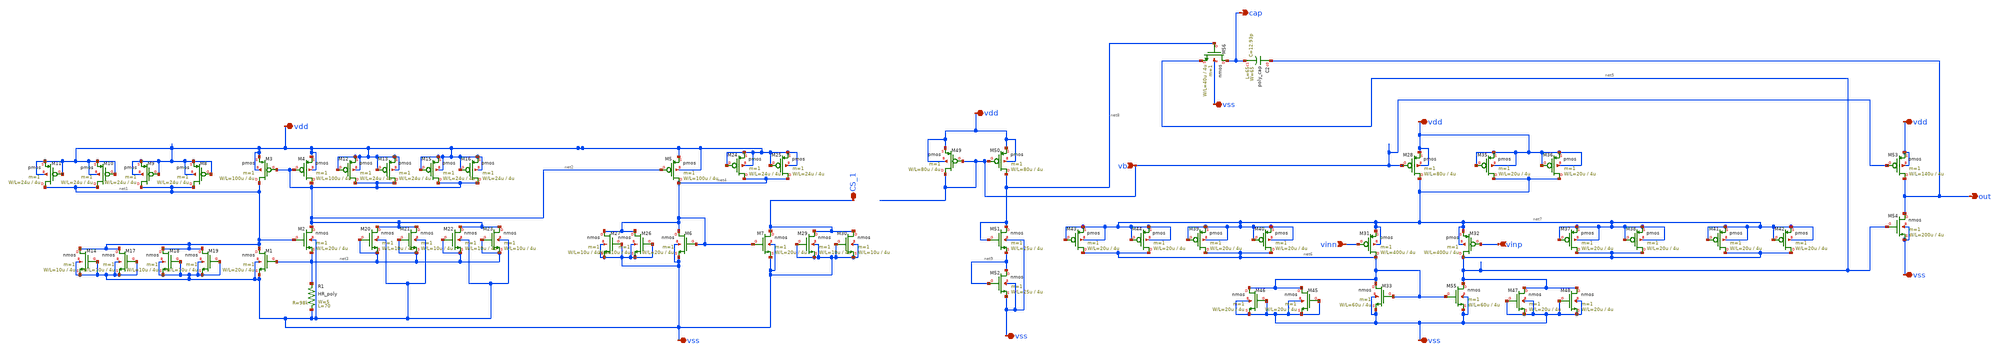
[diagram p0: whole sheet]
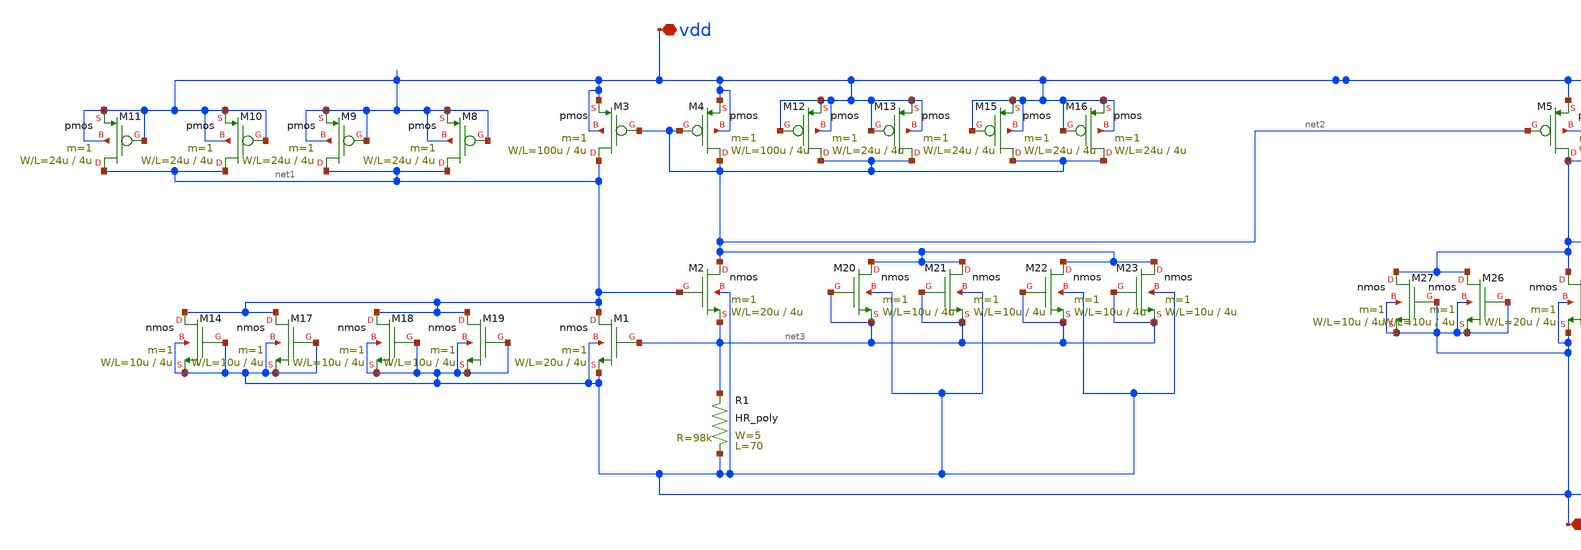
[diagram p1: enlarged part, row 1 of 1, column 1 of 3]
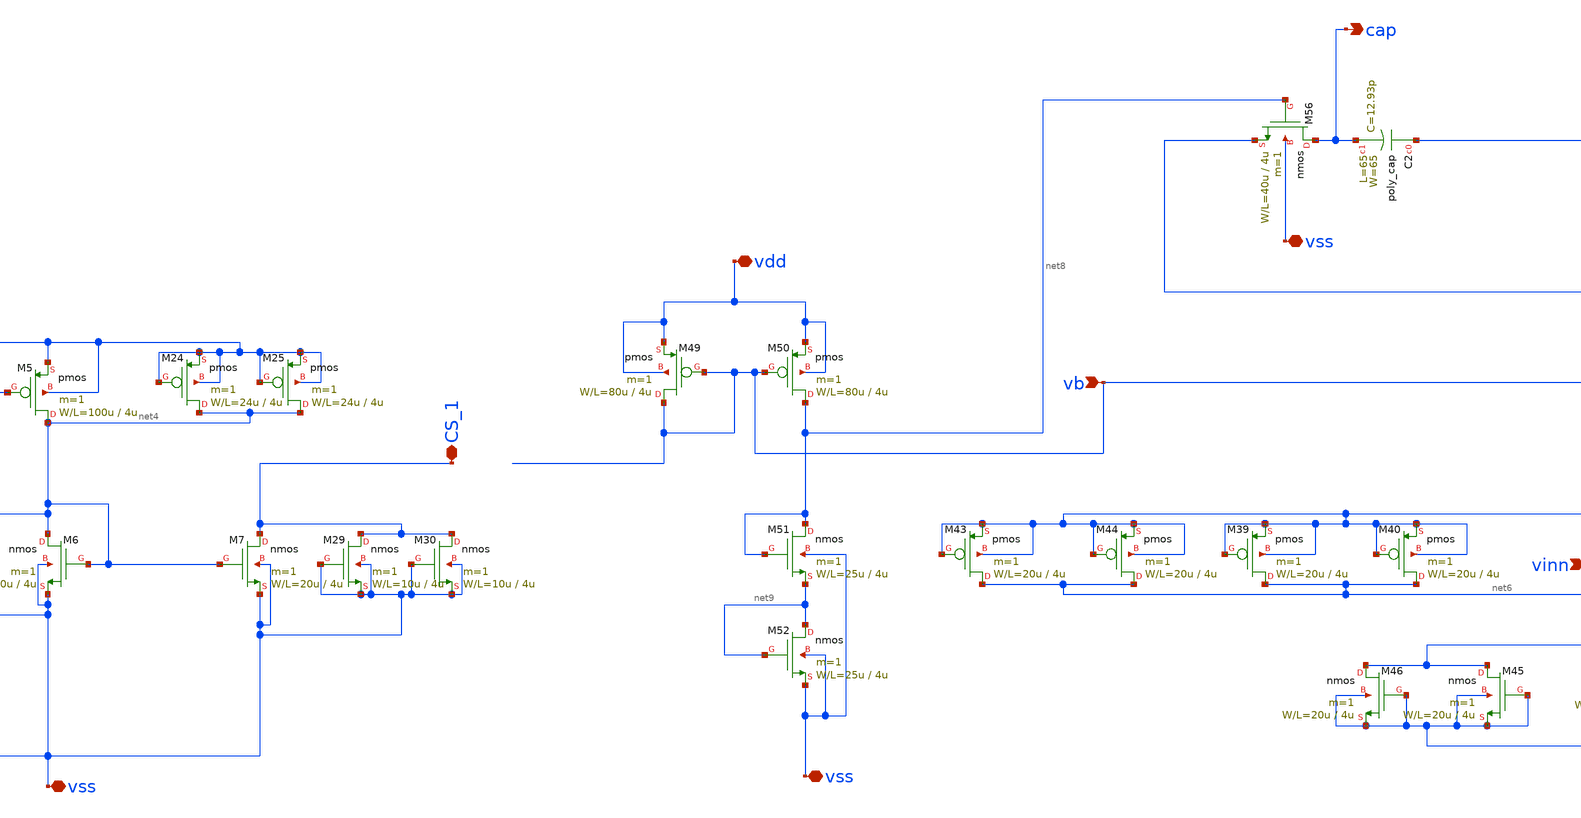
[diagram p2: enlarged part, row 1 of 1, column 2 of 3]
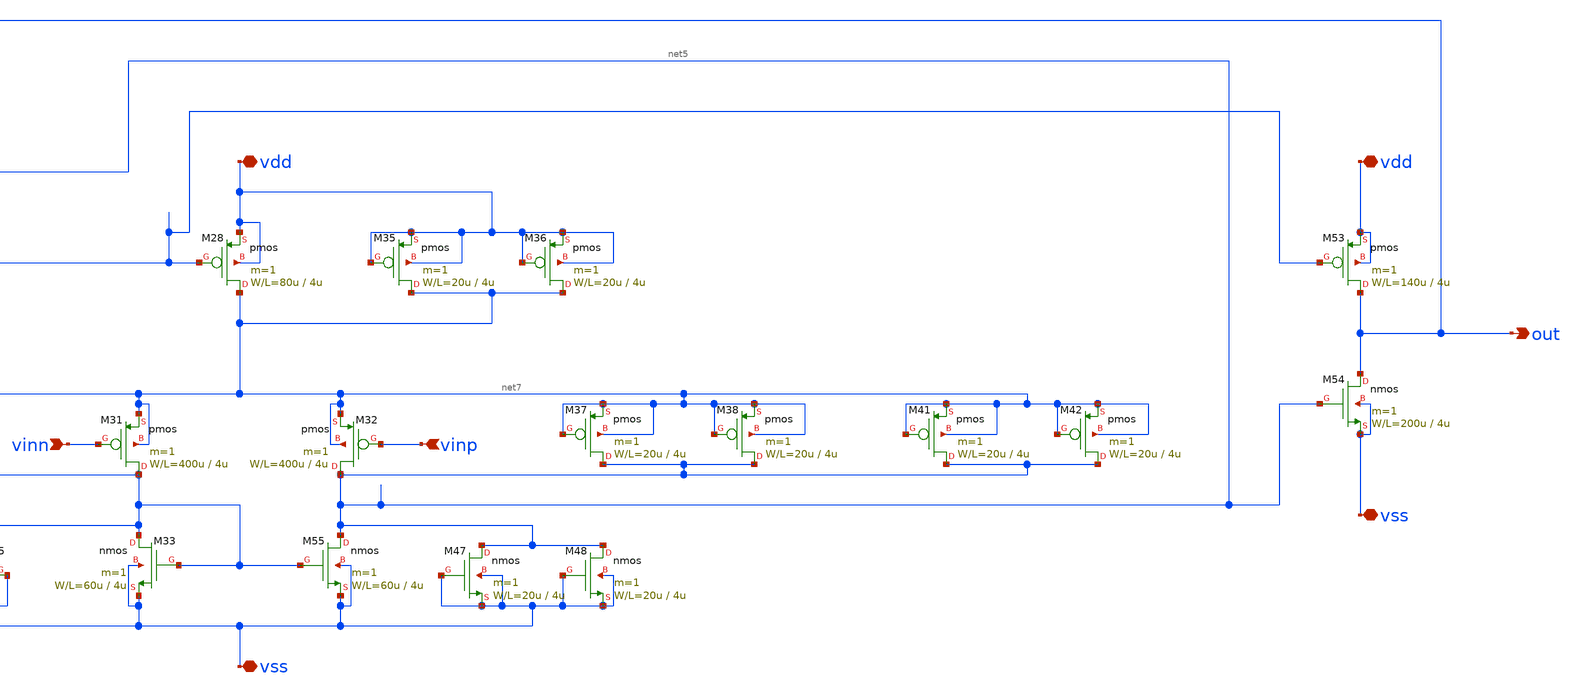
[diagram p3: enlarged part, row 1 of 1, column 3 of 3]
** sch_path: Vol.2/files/08/xschem/ichiken/opamp_ichiken_v3.sch
**.subckt opamp_ichiken_v3 vdd vss vinn vinp vb cap vdd vss vss vdd vss vdd vss out CS_1
*.iopin vdd
*.iopin vss
*.ipin vinn
*.ipin vinp
*.ipin vb
*.opin cap
*.iopin vdd
*.iopin vss
*.iopin vss
*.iopin vdd
*.iopin vss
*.iopin vdd
*.iopin vss
*.opin out
*.iopin CS_1
M4 net2 net2 vdd vdd pmos L=4u W=100u m=1
M3 net1 net2 vdd vdd pmos L=4u W=100u m=1
M2 net2 net1 net3 vss nmos L=4u W=20u m=1
M1 net1 net3 vss vss nmos L=4u W=20u m=1
M5 net4 net2 vdd vdd pmos L=4u W=100u m=1
M6 net4 net4 vss vss nmos L=4u W=20u m=1
M7 CS_1 net4 vss vss nmos L=4u W=20u m=1
M8 net1 vdd vdd vdd pmos L=4u W=24u m=1
M9 net1 vdd vdd vdd pmos L=4u W=24u m=1
M10 net1 vdd vdd vdd pmos L=4u W=24u m=1
M11 net1 vdd vdd vdd pmos L=4u W=24u m=1
M13 net2 vdd vdd vdd pmos L=4u W=24u m=1
M12 net2 vdd vdd vdd pmos L=4u W=24u m=1
M15 net2 vdd vdd vdd pmos L=4u W=24u m=1
M16 net2 vdd vdd vdd pmos L=4u W=24u m=1
M24 net4 vdd vdd vdd pmos L=4u W=24u m=1
M25 net4 vdd vdd vdd pmos L=4u W=24u m=1
M26 net4 vss vss vss nmos L=4u W=10u m=1
M27 net4 vss vss vss nmos L=4u W=10u m=1
M29 CS_1 vss vss vss nmos L=4u W=10u m=1
M30 CS_1 vss vss vss nmos L=4u W=10u m=1
M28 net7 vb vdd vdd pmos L=4u W=80u m=1
M31 net6 vinn net7 net7 pmos L=4u W=400u m=1
M32 net5 vinp net7 net7 pmos L=4u W=400u m=1
M33 net6 net6 vss vss nmos L=4u W=60u m=1
M35 net7 vdd vdd vdd pmos L=4u W=20u m=1
M36 net7 vdd vdd vdd pmos L=4u W=20u m=1
M37 net5 net7 net7 net7 pmos L=4u W=20u m=1
M38 net5 net7 net7 net7 pmos L=4u W=20u m=1
M39 net6 net7 net7 net7 pmos L=4u W=20u m=1
M40 net6 net7 net7 net7 pmos L=4u W=20u m=1
M41 net5 net7 net7 net7 pmos L=4u W=20u m=1
M42 net5 net7 net7 net7 pmos L=4u W=20u m=1
M43 net6 net7 net7 net7 pmos L=4u W=20u m=1
M44 net6 net7 net7 net7 pmos L=4u W=20u m=1
M45 net6 vss vss vss nmos L=4u W=20u m=1
M46 net6 vss vss vss nmos L=4u W=20u m=1
M47 net5 vss vss vss nmos L=4u W=20u m=1
M48 net5 vss vss vss nmos L=4u W=20u m=1
M49 vb vb vdd vdd pmos L=4u W=80u m=1
M51 net8 net8 net9 vss nmos L=4u W=25u m=1
M52 net9 net9 vss vss nmos L=4u W=25u m=1
M53 out vb vdd vdd pmos L=4u W=140u m=1
M54 out net5 vss vss nmos L=4u W=200u m=1
M55 net5 net6 vss vss nmos L=4u W=60u m=1
M56 cap net8 net5 vss nmos L=4u W=40u m=1
R1 vss net3 HR_poly W=5 L=70
M20 net2 net3 net3 vss nmos L=4u W=10u m=1
M21 net2 net3 net3 vss nmos L=4u W=10u m=1
M22 net2 net3 net3 vss nmos L=4u W=10u m=1
M23 net2 net3 net3 vss nmos L=4u W=10u m=1
M14 net1 vss vss vss nmos L=4u W=10u m=1
M17 net1 vss vss vss nmos L=4u W=10u m=1
M18 net1 vss vss vss nmos L=4u W=10u m=1
M19 net1 vss vss vss nmos L=4u W=10u m=1
M50 net8 vb vdd vdd pmos L=4u W=80u m=1
C2 out cap poly_cap W=65 L=65
**.ends
.end
